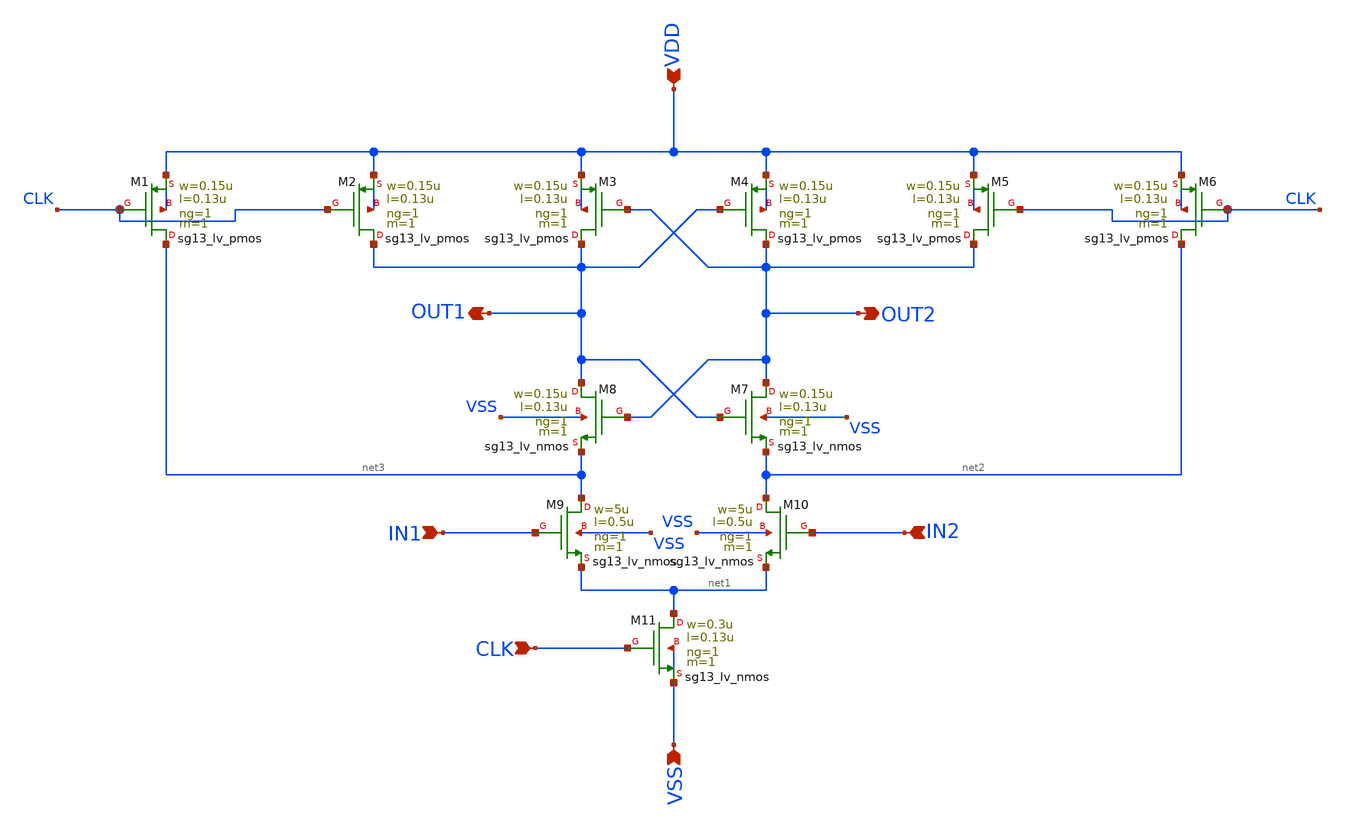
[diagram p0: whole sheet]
** sch_path: designs/comparator/comparator.sch
**.subckt comparator CLK IN1 IN2 OUT2 OUT1 VSS VDD
*.ipin CLK
*.ipin IN1
*.ipin IN2
*.opin OUT2
*.opin OUT1
*.ipin VSS
*.ipin VDD
XM1 net3 CLK VDD VDD sg13_lv_pmos w=0.15u l=0.13u ng=1 m=1 mm_ok=1
XM2 OUT1 CLK VDD VDD sg13_lv_pmos w=0.15u l=0.13u ng=1 m=1 mm_ok=1
XM3 OUT1 OUT2 VDD VDD sg13_lv_pmos w=0.15u l=0.13u ng=1 m=1 mm_ok=1
XM4 OUT2 OUT1 VDD VDD sg13_lv_pmos w=0.15u l=0.13u ng=1 m=1 mm_ok=1
XM5 OUT2 CLK VDD VDD sg13_lv_pmos w=0.15u l=0.13u ng=1 m=1 mm_ok=1
XM6 net2 CLK VDD VDD sg13_lv_pmos w=0.15u l=0.13u ng=1 m=1 mm_ok=1
XM7 OUT2 OUT1 net2 VSS sg13_lv_nmos w=0.15u l=0.13u ng=1 m=1 mm_ok=1
XM8 OUT1 OUT2 net3 VSS sg13_lv_nmos w=0.15u l=0.13u ng=1 m=1 mm_ok=1
XM9 net3 IN1 net1 VSS sg13_lv_nmos w=5u l=0.5u ng=1 m=1 mm_ok=1
XM10 net2 IN2 net1 VSS sg13_lv_nmos w=5u l=0.5u ng=1 m=1 mm_ok=1
XM11 net1 CLK VSS VSS sg13_lv_nmos w=0.3u l=0.13u ng=1 m=1 mm_ok=1
**.ends
.end
